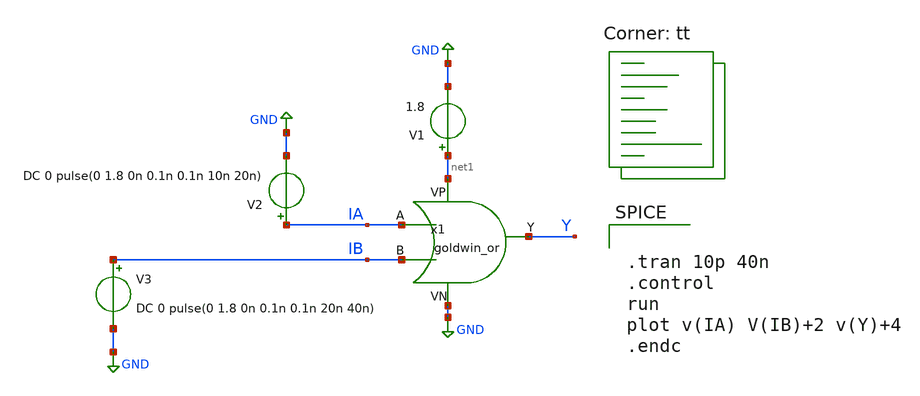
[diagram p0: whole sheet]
** sch_path: APIC-UTS/schematic/goldwin_or/tb_goldwin_or.sch
**.subckt tb_goldwin_or
V1 net1 GND 1.8
V2 IA GND DC 0 pulse(0 1.8 0n 0.1n 0.1n 10n 20n)
V3 IB GND DC 0 pulse(0 1.8 0n 0.1n 0.1n 20n 40n)
x1 IA IB Y net1 GND goldwin_or
**** begin user architecture code


.tran 10p 40n
.control
run
plot v(IA) V(IB)+2 v(Y)+4
.endc


.lib $::SKYWATER_MODELS/sky130.lib.spice tt
**** end user architecture code
**.ends

* expanding   symbol:  goldwin_or.sym # of pins=5
** sym_path: APIC-UTS/schematic/goldwin_or/goldwin_or.sym
** sch_path: APIC-UTS/schematic/goldwin_or/goldwin_or.sch
.subckt goldwin_or A B Y VP VN
*.ipin A
*.ipin B
*.opin Y
*.ipin VP
*.ipin VN
XM1 net1 A VN VN sky130_fd_pr__nfet_01v8 L=0.15 W=1 nf=1 ad='int((nf+1)/2) * W/nf * 0.29' as='int((nf+2)/2) * W/nf * 0.29'
+ pd='2*int((nf+1)/2) * (W/nf + 0.29)' ps='2*int((nf+2)/2) * (W/nf + 0.29)' nrd='0.29 / W' nrs='0.29 / W'
+ sa=0 sb=0 sd=0 mult=1 m=1
XM4 net1 B VN VN sky130_fd_pr__nfet_01v8 L=0.15 W=1 nf=1 ad='int((nf+1)/2) * W/nf * 0.29' as='int((nf+2)/2) * W/nf * 0.29'
+ pd='2*int((nf+1)/2) * (W/nf + 0.29)' ps='2*int((nf+2)/2) * (W/nf + 0.29)' nrd='0.29 / W' nrs='0.29 / W'
+ sa=0 sb=0 sd=0 mult=1 m=1
XM6 Y net1 VN VN sky130_fd_pr__nfet_01v8 L=0.15 W=1 nf=1 ad='int((nf+1)/2) * W/nf * 0.29' as='int((nf+2)/2) * W/nf * 0.29'
+ pd='2*int((nf+1)/2) * (W/nf + 0.29)' ps='2*int((nf+2)/2) * (W/nf + 0.29)' nrd='0.29 / W' nrs='0.29 / W'
+ sa=0 sb=0 sd=0 mult=1 m=1
XM2 net2 A VP VP sky130_fd_pr__pfet_01v8 L=0.15 W=3 nf=1 ad='int((nf+1)/2) * W/nf * 0.29' as='int((nf+2)/2) * W/nf * 0.29'
+ pd='2*int((nf+1)/2) * (W/nf + 0.29)' ps='2*int((nf+2)/2) * (W/nf + 0.29)' nrd='0.29 / W' nrs='0.29 / W'
+ sa=0 sb=0 sd=0 mult=1 m=1
XM3 net1 B net2 VP sky130_fd_pr__pfet_01v8 L=0.15 W=3 nf=1 ad='int((nf+1)/2) * W/nf * 0.29' as='int((nf+2)/2) * W/nf * 0.29'
+ pd='2*int((nf+1)/2) * (W/nf + 0.29)' ps='2*int((nf+2)/2) * (W/nf + 0.29)' nrd='0.29 / W' nrs='0.29 / W'
+ sa=0 sb=0 sd=0 mult=1 m=1
XM5 Y net1 VP VP sky130_fd_pr__pfet_01v8 L=0.15 W=3 nf=1 ad='int((nf+1)/2) * W/nf * 0.29' as='int((nf+2)/2) * W/nf * 0.29'
+ pd='2*int((nf+1)/2) * (W/nf + 0.29)' ps='2*int((nf+2)/2) * (W/nf + 0.29)' nrd='0.29 / W' nrs='0.29 / W'
+ sa=0 sb=0 sd=0 mult=1 m=1
.ends

.GLOBAL GND
.end
